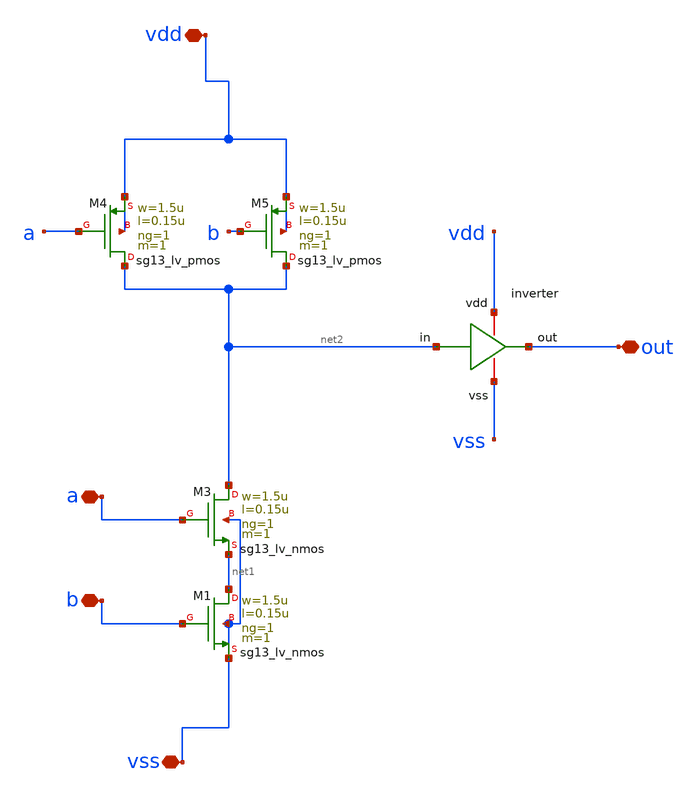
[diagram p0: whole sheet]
** sch_path: design/blocks/andgate/schematic/andgate.sch
**.subckt andgate b a vdd vss out
*.iopin b
*.iopin a
*.iopin vdd
*.iopin vss
*.iopin out
XM1 net1 b vss vss sg13_lv_nmos w=1.5u l=0.15u ng=1 m=1 mm_ok=1
XM4 net2 a vdd vdd sg13_lv_pmos w=1.5u l=0.15u ng=1 m=1 mm_ok=1
x1 vdd out net2 vss inverter
XM3 net2 a net1 vss sg13_lv_nmos w=1.5u l=0.15u ng=1 m=1 mm_ok=1
XM5 net2 b vdd vdd sg13_lv_pmos w=1.5u l=0.15u ng=1 m=1 mm_ok=1
**.ends

* expanding   symbol:  blocks/inverter/schematic/inverter.sym # of pins=4
** sym_path: design/blocks/inverter/schematic/inverter.sym
** sch_path: design/blocks/inverter/schematic/inverter.sch
.subckt inverter vdd out in vss
*.iopin vdd
*.iopin out
*.iopin vss
*.iopin in
XM1 out in vss vss sky130_fd_pr__nfet_01v8 L=0.15 W=0.75 nf=1 ad='int((nf+1)/2) * W/nf * 0.29' as='int((nf+2)/2) * W/nf * 0.29'
+ pd='2*int((nf+1)/2) * (W/nf + 0.29)' ps='2*int((nf+2)/2) * (W/nf + 0.29)' nrd='0.29 / W' nrs='0.29 / W'
+ sa=0 sb=0 sd=0 mult=1 m=1
XM2 out in vdd vdd sky130_fd_pr__pfet_01v8 L=0.15 W=1.5 nf=1 ad='int((nf+1)/2) * W/nf * 0.29' as='int((nf+2)/2) * W/nf * 0.29'
+ pd='2*int((nf+1)/2) * (W/nf + 0.29)' ps='2*int((nf+2)/2) * (W/nf + 0.29)' nrd='0.29 / W' nrs='0.29 / W'
+ sa=0 sb=0 sd=0 mult=1 m=1
.ends

.end
